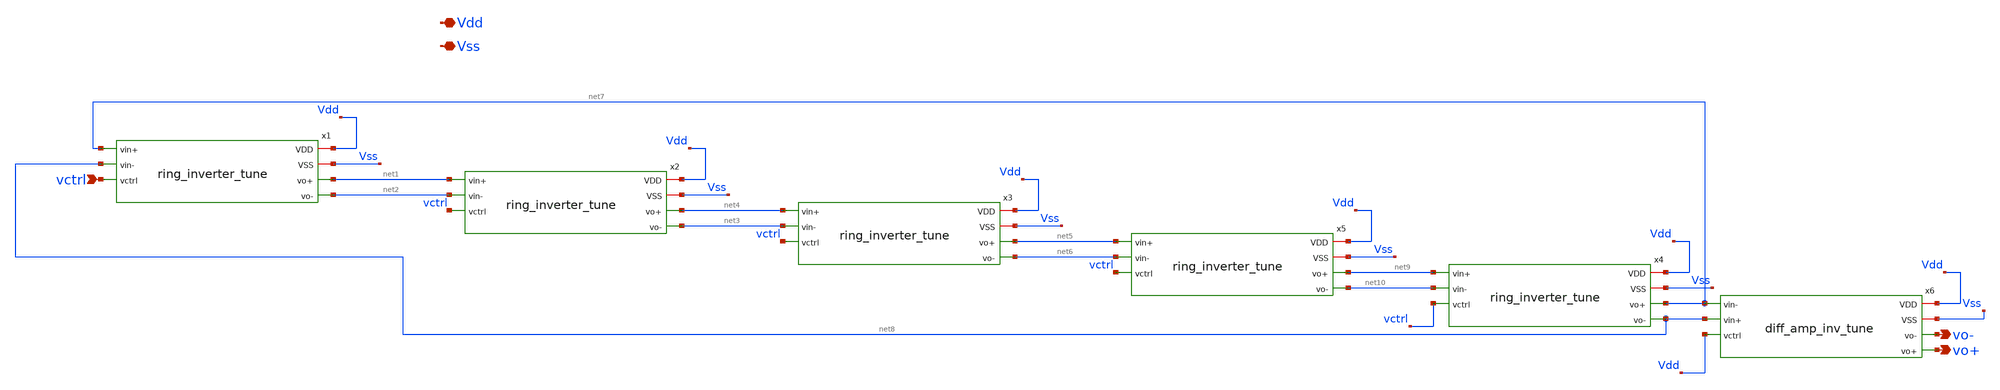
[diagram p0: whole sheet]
** sch_path: xschem/tuning/ring_oscillator_tune.sch
**.subckt ring_oscillator_tune Vdd Vss vctrl vo+ vo-
*.iopin Vdd
*.iopin Vss
*.ipin vctrl
*.opin vo+
*.opin vo-
x1 Vdd Vss net7 net1 net8 net2 vctrl ring_inverter_tune
x2 Vdd Vss net1 net4 net2 net3 vctrl ring_inverter_tune
x3 Vdd Vss net4 net5 net3 net6 vctrl ring_inverter_tune
x5 Vdd Vss net5 net9 net6 net10 vctrl ring_inverter_tune
x4 Vdd Vss net9 net7 net10 net8 vctrl ring_inverter_tune
x6 Vdd Vss vo- vo+ net7 net8 Vdd diff_amp_inv_tune
**.ends
.end
